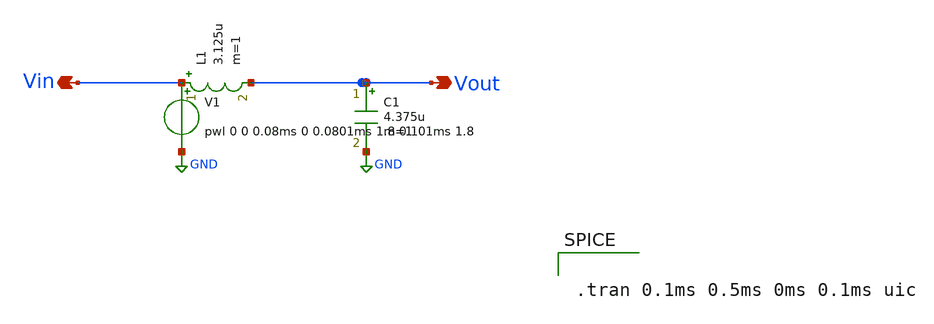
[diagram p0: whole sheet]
** sch_path: Current Sensor/untitled-8.sch
**.subckt untitled-8 Vin Vout
*.opin Vin
*.opin Vout
C1 Vout GND 4.375u m=1
L1 Vin Vout 3.125u m=1
V1 Vin GND pwl 0 0 0.08ms 0 0.0801ms 1.8 0.101ms 1.8
**** begin user architecture code


.tran 0.1ms 0.5ms 0ms 0.1ms uic


** opencircuitdesign pdks install
.lib $::SKYWATER_MODELS/sky130.lib.spice tt_mm


**** end user architecture code
**.ends
.GLOBAL GND
.end
